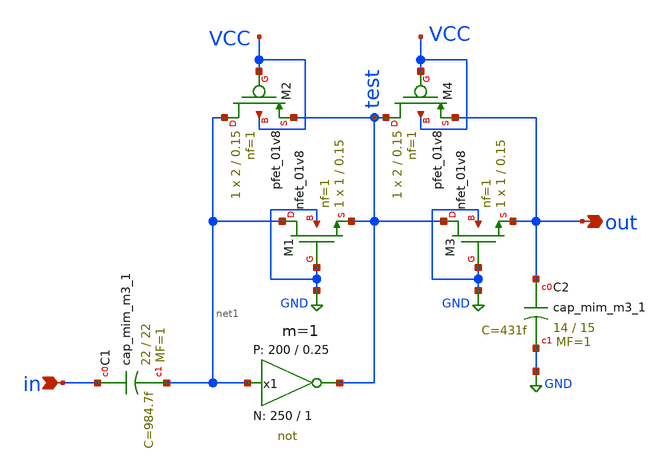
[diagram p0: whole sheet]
** sch_path: Amplifier_Inv/xschem/inv_sky130_a_v2.sch
* StefanSchippers/xschem_sky130/sky130_tests/not.sch:
* Copyright 2021 Stefan Frederik Schippers
* Licensed under the Apache License, Version 2.0 (the "License");
**.subckt inv_sky130_a_v2 in out
*.ipin in
*.opin out
x1 test net1 VCC VSS not W_N=250 L_N=1 W_P=200 L_P=0.25 m=1
XC2 out GND sky130_fd_pr__cap_mim_m3_1 W=14 L=15 MF=1 m=1
XC1 in net1 sky130_fd_pr__cap_mim_m3_1 W=22 L=22 MF=1 m=1
XM1 net1 GND test GND sky130_fd_pr__nfet_01v8 L=0.15 W=1 nf=1 ad='int((nf+1)/2) * W/nf * 0.29' as='int((nf+2)/2) * W/nf * 0.29'
+ pd='2*int((nf+1)/2) * (W/nf + 0.29)' ps='2*int((nf+2)/2) * (W/nf + 0.29)' nrd='0.29 / W' nrs='0.29 / W'
+ sa=0 sb=0 sd=0 mult=1 m=1
XM3 test GND out GND sky130_fd_pr__nfet_01v8 L=0.15 W=1 nf=1 ad='int((nf+1)/2) * W/nf * 0.29' as='int((nf+2)/2) * W/nf * 0.29'
+ pd='2*int((nf+1)/2) * (W/nf + 0.29)' ps='2*int((nf+2)/2) * (W/nf + 0.29)' nrd='0.29 / W' nrs='0.29 / W'
+ sa=0 sb=0 sd=0 mult=1 m=1
XM2 net1 VCC test VCC sky130_fd_pr__pfet_01v8 L=0.15 W=2 nf=1 ad='int((nf+1)/2) * W/nf * 0.29' as='int((nf+2)/2) * W/nf * 0.29'
+ pd='2*int((nf+1)/2) * (W/nf + 0.29)' ps='2*int((nf+2)/2) * (W/nf + 0.29)' nrd='0.29 / W' nrs='0.29 / W'
+ sa=0 sb=0 sd=0 mult=1 m=1
XM4 test VCC out VCC sky130_fd_pr__pfet_01v8 L=0.15 W=2 nf=1 ad='int((nf+1)/2) * W/nf * 0.29' as='int((nf+2)/2) * W/nf * 0.29'
+ pd='2*int((nf+1)/2) * (W/nf + 0.29)' ps='2*int((nf+2)/2) * (W/nf + 0.29)' nrd='0.29 / W' nrs='0.29 / W'
+ sa=0 sb=0 sd=0 mult=1 m=1
**.ends

* expanding   symbol:  sky130_tests/not.sym # of pins=2
** sym_path: sky130_tests/not.sym
** sch_path: sky130_tests/not.sch
.subckt not y a VCCPIN VSSPIN     W_N=1 L_N=0.15 W_P=2 L_P=0.15
*.opin y
*.ipin a
XM1 DN a VSSPIN VSSPIN sky130_fd_pr__nfet_01v8 L=L_N W=W_N nf=1 ad='int((1 + 1)/2) * W_N / 1 * 0.29'
+ as='int((1 + 2)/2) * W_N / 1 * 0.29' pd='2*int((1 + 1)/2) * (W_N / 1 + 0.29)' ps='2*int((1 + 2)/2) * (W_N / 1 + 0.29)'
+ nrd='0.29 / W_N ' nrs='0.29 / W_N ' sa=0 sb=0 sd=0 mult=1 m=1
XM2 DP a VCCPIN VCCPIN sky130_fd_pr__pfet_01v8 L=L_P W=W_P nf=1 ad='int((nf+1)/2) * W/nf * 0.29' as='int((nf+2)/2) * W/nf * 0.29'
+ pd='2*int((nf+1)/2) * (W/nf + 0.29)' ps='2*int((nf+2)/2) * (W/nf + 0.29)' nrd='0.29 / W' nrs='0.29 / W'
+ sa=0 sb=0 sd=0 mult=1 m=1
Vmeas DP y 0
.save i(vmeas)
Vmeas1 y DN 0
.save i(vmeas1)
.save v(dp)
.save v(dn)
.ends

.GLOBAL GND
.end
